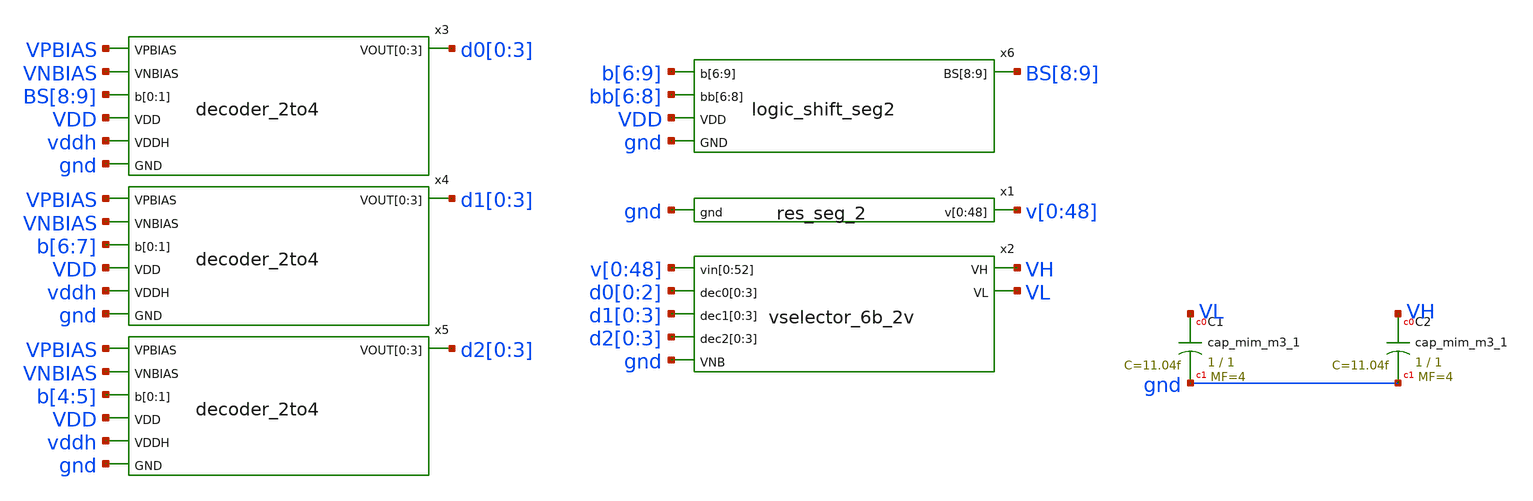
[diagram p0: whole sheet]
** sch_path: xschem/res_seg_2-tb.sch
.lib $::SKYWATER_MODELS/sky130.lib.spice tt
.include $::SKYWATER_STDCELLS/sky130_fd_sc_hd.spice

**.subckt res_seg_2-tb
x1 v[0] v[1] v[2] v[3] v[4] v[5] v[6] v[7] v[8] v[9] v[10] v[11] v[12] v[13] v[14] v[15] v[16] v[17]
+ v[18] v[19] v[20] v[21] v[22] v[23] v[24] v[25] v[26] v[27] v[28] v[29] v[30] v[31] v[32] v[33] v[34]
+ v[35] v[36] v[37] v[38] v[39] v[40] v[41] v[42] v[43] v[44] v[45] v[46] v[47] v[48] gnd res_seg_2
x2 v[0] v[1] v[2] v[3] v[4] v[5] v[6] v[7] v[8] v[9] v[10] v[11] v[12] v[13] v[14] v[15] v[16] v[17]
+ v[18] v[19] v[20] v[21] v[22] v[23] v[24] v[25] v[26] v[27] v[28] v[29] v[30] v[31] v[32] v[33] v[34]
+ v[35] v[36] v[37] v[38] v[39] v[40] v[41] v[42] v[43] v[44] v[45] v[46] v[47] v[48] v[0] v[1] v[2] v[3]
+ d0[0] d0[1] d0[2] d0[0] d1[0] d1[1] d1[2] d1[3] d2[0] d2[1] d2[2] d2[3] VH VL gnd vselector_6b_2v
XC1 VL gnd sky130_fd_pr__cap_mim_m3_1 W=1 L=1 MF=4 m=4
XC2 VH gnd sky130_fd_pr__cap_mim_m3_1 W=1 L=1 MF=4 m=4
x3 VPBIAS VNBIAS BS[8] BS[9] d0[0] d0[1] d0[2] d0[3] VDD vddh gnd decoder_2to4
x4 VPBIAS VNBIAS b[6] b[7] d1[0] d1[1] d1[2] d1[3] VDD vddh gnd decoder_2to4
x5 VPBIAS VNBIAS b[4] b[5] d2[0] d2[1] d2[2] d2[3] VDD vddh gnd decoder_2to4
x6 b[6] b[7] b[8] b[9] bb[6] bb[7] bb[8] BS[8] BS[9] VDD gnd logic_shift_seg2
**** begin user architecture code



  .option wnflag=1
  .option safecurrents
  .options reltol=1e-5
  .option klu
  ********************Static Voltage Sources***************************
  Vddh vddh gnd dc 5.5
  Vdd vdd gnd dc 1.8

  .param vpb_val = 2.98 vnb_val=1.506
  Vp vpbias gnd dc vpb_val
  Vn vnbias gnd dc vnb_val

  V52 v[48] gnd dc 4.0164
  v0 v[0] gnd dc 1.0442
  ********************Dynamic Voltage Sources***************************
  *******Calculation**********
  .param base_f=100e3 base_t={1/base_f} base_th={base_t/2} base_d={base_th}
  .param b4_th={base_th} b4_t={b4_th*2}
  .param b5_th={b4_th*2} b5_t={b5_th*2}
  .param b6_th={b5_th*2} b6_t={b6_th*2}
  .param b7_th={b6_th*2} b7_t={b7_th*2}
  .param b8_th={b7_th*2} b8_t={b8_th*2}
  .param b9_th={b8_th*2} b9_t={b9_th*2}

  .param delay_6 = {base_d+b5_t}
  .param delay_7 = {delay_6}
  .param delay_8 = {delay_7+b7_th}
  .param delay_9 = {delay_8+b8_th}
  *******Signals**********
  .param vhi=1.8
  Vb4  b[4]  gnd pulse({vhi} 0 {base_d} 1n 1n {b4_th} {b4_t})
  Vb5  b[5]  gnd pulse({vhi} 0 {base_d} 1n 1n {b5_th} {b5_t})
  Vb6  b[6]  gnd pulse({vhi} 0 {delay_6} 1n 1n {b6_th} {b6_t})
  Vb7  b[7]  gnd pulse(0 {vhi} {delay_7} 1n 1n {b7_th} {b7_t})
  Vb8  b[8]  gnd pulse(0 {vhi} {delay_8} 1n 1n {b8_th} {b8_t})
  Vb9  b[9]  gnd pulse(0 {vhi} {delay_9} 1n 1n {b9_th} {b9_t})

  Vbb4  bb[4]  gnd pulse(0 {vhi} {base_d} 1n 1n {b4_th} {b4_t})
  Vbb5  bb[5]  gnd pulse(0 {vhi} {base_d} 1n 1n {b5_th} {b5_t})
  Vbb6  bb[6]  gnd pulse(0 {vhi} {delay_6} 1n 1n {b6_th} {b6_t})
  Vbb7  bb[7]  gnd pulse({vhi} 0 {delay_7} 1n 1n {b7_th} {b7_t})
  Vbb8  bb[8]  gnd pulse({vhi} 0 {delay_8} 1n 1n {b8_th} {b8_t})
  Vbb9  bb[9]  gnd pulse({vhi} 0 {delay_9} 1n 1n {b9_th} {b9_t})
  ********************Simulation Commands*****************************
  .control
     reset
     set num_threads=50
     save all
     tran 10n 260u
     write res_seg_2-tb.raw
     set appendwrite
*    quit 0
  .endc



**** end user architecture code
**.ends

* expanding   symbol:  res_seg_2.sym # of pins=2
** sym_path: xschem/res_seg_2.sym
** sch_path: xschem/res_seg_2.sch
.subckt res_seg_2 v[0] v[1] v[2] v[3] v[4] v[5] v[6] v[7] v[8] v[9] v[10] v[11] v[12] v[13] v[14]
+ v[15] v[16] v[17] v[18] v[19] v[20] v[21] v[22] v[23] v[24] v[25] v[26] v[27] v[28] v[29] v[30] v[31]
+ v[32] v[33] v[34] v[35] v[36] v[37] v[38] v[39] v[40] v[41] v[42] v[43] v[44] v[45] v[46] v[47] v[48] gnd
*.opin
*+ v[0],v[1],v[2],v[3],v[4],v[5],v[6],v[7],v[8],v[9],v[10],v[11],v[12],v[13],v[14],v[15],v[16],v[17],v[18],v[19],v[20],v[21],v[22],v[23],v[24],v[25],v[26],v[27],v[28],v[29],v[30],v[31],v[32],v[33],v[34],v[35],v[36],v[37],v[38],v[39],v[40],v[41],v[42],v[43],v[44],v[45],v[46],v[47],v[48]
*.ipin gnd
XR1 v[1] v[0] gnd sky130_fd_pr__res_xhigh_po_0p35 L=1.9570 mult=1 m=1
XR2 v[2] v[1] gnd sky130_fd_pr__res_xhigh_po_0p35 L=1.7348 mult=1 m=1
XR3 v[3] v[2] gnd sky130_fd_pr__res_xhigh_po_0p35 L=1.5639 mult=1 m=1
XR4 v[4] v[3] gnd sky130_fd_pr__res_xhigh_po_0p35 L=1.4442 mult=1 m=1
XR5 v[5] v[4] gnd sky130_fd_pr__res_xhigh_po_0p35 L=1.3417 mult=1 m=1
XR6 v[6] v[5] gnd sky130_fd_pr__res_xhigh_po_0p35 L=1.2648 mult=1 m=1
XR7 v[7] v[6] gnd sky130_fd_pr__res_xhigh_po_0p35 L=1.1964 mult=1 m=1
XR8 v[8] v[7] gnd sky130_fd_pr__res_xhigh_po_0p35 L=1.1366 mult=1 m=1
XR9 v[9] v[8] gnd sky130_fd_pr__res_xhigh_po_0p35 L=1.0853 mult=1 m=1
XR10 v[10] v[9] gnd sky130_fd_pr__res_xhigh_po_0p35 L=1.0511 mult=1 m=1
XR11 v[11] v[10] gnd sky130_fd_pr__res_xhigh_po_0p35 L=1.0169 mult=1 m=1
XR12 v[12] v[11] gnd sky130_fd_pr__res_xhigh_po_0p35 L=0.9828 mult=1 m=1
XR13 v[13] v[12] gnd sky130_fd_pr__res_xhigh_po_0p35 L=0.9571 mult=1 m=1
XR14 v[14] v[13] gnd sky130_fd_pr__res_xhigh_po_0p35 L=0.94 mult=1 m=1
XR15 v[15] v[14] gnd sky130_fd_pr__res_xhigh_po_0p35 L=0.9144 mult=1 m=1
XR16 v[16] v[15] gnd sky130_fd_pr__res_xhigh_po_0p35 L=0.8888 mult=1 m=1
XR17 v[17] v[16] gnd sky130_fd_pr__res_xhigh_po_0p35 L=0.8802 mult=1 m=1
XR18 v[18] v[17] gnd sky130_fd_pr__res_xhigh_po_0p35 L=0.8717 mult=1 m=1
XR19 v[19] v[18] gnd sky130_fd_pr__res_xhigh_po_0p35 L=0.8546 mult=1 m=1
XR20 v[20] v[19] gnd sky130_fd_pr__res_xhigh_po_0p35 L=0.8375 mult=1 m=1
XR22 v[22] v[21] gnd sky130_fd_pr__res_xhigh_po_0p35 L=0.8289 mult=1 m=1
XR23 v[23] v[22] gnd sky130_fd_pr__res_xhigh_po_0p35 L=0.8204 mult=1 m=1
XR24 v[24] v[23] gnd sky130_fd_pr__res_xhigh_po_0p35 L=0.8118 mult=1 m=1
XR33 v[33] v[32] gnd sky130_fd_pr__res_xhigh_po_0p35 L=0.8204 mult=1 m=1
XR35 v[35] v[34] gnd sky130_fd_pr__res_xhigh_po_0p35 L=0.8289 mult=1 m=1
XR36 v[36] v[35] gnd sky130_fd_pr__res_xhigh_po_0p35 L=0.8375 mult=1 m=1
XR38 v[38] v[37] gnd sky130_fd_pr__res_xhigh_po_0p35 L=0.8631 mult=1 m=1
XR40 v[40] v[39] gnd sky130_fd_pr__res_xhigh_po_0p35 L=0.8888 mult=1 m=1
XR41 v[41] v[40] gnd sky130_fd_pr__res_xhigh_po_0p35 L=0.8973 mult=1 m=1
XR42 v[42] v[41] gnd sky130_fd_pr__res_xhigh_po_0p35 L=0.9144 mult=1 m=1
XR43 v[43] v[42] gnd sky130_fd_pr__res_xhigh_po_0p35 L=0.94 mult=1 m=1
XR44 v[44] v[43] gnd sky130_fd_pr__res_xhigh_po_0p35 L=0.9571 mult=1 m=1
XR45 v[45] v[44] gnd sky130_fd_pr__res_xhigh_po_0p35 L=0.9828 mult=1 m=1
XR46 v[46] v[45] gnd sky130_fd_pr__res_xhigh_po_0p35 L=1.0084 mult=1 m=1
XR47 v[47] v[46] gnd sky130_fd_pr__res_xhigh_po_0p35 L=1.0426 mult=1 m=1
XR48 v[48] v[47] gnd sky130_fd_pr__res_xhigh_po_0p35 L=1.0853 mult=1 m=1
XR37 v[37] v[36] gnd sky130_fd_pr__res_xhigh_po_0p35 L=0.846 mult=1 m=1
XR21 v[21] v[20] gnd sky130_fd_pr__res_xhigh_po_0p35 L=0.8375 mult=1 m=1
XR25 v[25] v[24] gnd sky130_fd_pr__res_xhigh_po_0p35 L=0.8118 mult=1 m=1
XR26 v[26] v[25] gnd sky130_fd_pr__res_xhigh_po_0p35 L=0.8118 mult=1 m=1
XR27 v[27] v[26] gnd sky130_fd_pr__res_xhigh_po_0p35 L=0.8033 mult=1 m=1
XR28 v[28] v[27] gnd sky130_fd_pr__res_xhigh_po_0p35 L=0.8118 mult=1 m=1
XR29 v[29] v[28] gnd sky130_fd_pr__res_xhigh_po_0p35 L=0.8033 mult=1 m=1
XR30 v[30] v[29] gnd sky130_fd_pr__res_xhigh_po_0p35 L=0.8033 mult=1 m=1
XR31 v[31] v[30] gnd sky130_fd_pr__res_xhigh_po_0p35 L=0.8118 mult=1 m=1
XR32 v[32] v[31] gnd sky130_fd_pr__res_xhigh_po_0p35 L=0.8118 mult=1 m=1
XR34 v[34] v[33] gnd sky130_fd_pr__res_xhigh_po_0p35 L=0.8204 mult=1 m=1
XR39 v[39] v[38] gnd sky130_fd_pr__res_xhigh_po_0p35 L=0.8631 mult=1 m=1
.ends


* expanding   symbol:  vselector_6b_2v.sym # of pins=7
** sym_path: xschem/vselector_6b_2v.sym
** sch_path: xschem/vselector_6b_2v.sch
.subckt vselector_6b_2v vin[0] vin[1] vin[2] vin[3] vin[4] vin[5] vin[6] vin[7] vin[8] vin[9]
+ vin[10] vin[11] vin[12] vin[13] vin[14] vin[15] vin[16] vin[17] vin[18] vin[19] vin[20] vin[21] vin[22]
+ vin[23] vin[24] vin[25] vin[26] vin[27] vin[28] vin[29] vin[30] vin[31] vin[32] vin[33] vin[34] vin[35]
+ vin[36] vin[37] vin[38] vin[39] vin[40] vin[41] vin[42] vin[43] vin[44] vin[45] vin[46] vin[47] vin[48]
+ vin[49] vin[50] vin[51] vin[52] dec0[0] dec0[1] dec0[2] dec0[3] dec1[0] dec1[1] dec1[2] dec1[3] dec2[0]
+ dec2[1] dec2[2] dec2[3] VH VL VNB
*.ipin
*+ vin[0],vin[1],vin[2],vin[3],vin[4],vin[5],vin[6],vin[7],vin[8],vin[9],vin[10],vin[11],vin[12],vin[13],vin[14],vin[15],vin[16],vin[17],vin[18],vin[19],vin[20],vin[21],vin[22],vin[23],vin[24],vin[25],vin[26],vin[27],vin[28],vin[29],vin[30],vin[31],vin[32],vin[33],vin[34],vin[35],vin[36],vin[37],vin[38],vin[39],vin[40],vin[41],vin[42],vin[43],vin[44],vin[45],vin[46],vin[47],vin[48],vin[49],vin[50],vin[51],vin[52]
*.opin VH
*.ipin VNB
*.ipin dec0[0],dec0[1],dec0[2],dec0[3]
*.opin VL
*.ipin dec1[0],dec1[1],dec1[2],dec1[3]
*.ipin dec2[0],dec2[1],dec2[2],dec2[3]
x1 vin[0] vin[1] vin[2] vin[3] vin[4] vin[5] vin[6] vin[7] vin[8] vin[9] vin[10] vin[11] vin[12]
+ vin[13] vin[14] vin[15] vin[16] vin[17] vin[18] vin[19] vin[20] vin[21] vin[22] vin[23] vin[24] vin[25]
+ vin[26] vin[27] vin[28] vin[29] vin[30] vin[31] vin[32] vin[33] vin[34] vin[35] vin[36] vin[37] vin[38]
+ vin[39] vin[40] vin[41] vin[42] vin[43] vin[44] vin[45] vin[46] vin[47] vin[48] vin[49] vin[50] vin[51]
+ vin[52] dec0[0] dec0[1] dec0[2] dec0[3] dec0[0] vout1[0] vout1[1] vout1[2] vout1[3] vout1[4] vout1[5]
+ vout1[6] vout1[7] vout1[8] vout1[9] vout1[10] vout1[11] vout1[12] vout1[13] vout1[14] vout1[15] vout1[16]
+ VNB vselector_6b_2v_stage_1
x2 vout1[0] vout1[1] vout1[2] vout1[3] vout1[4] vout1[5] vout1[6] vout1[7] vout1[8] vout1[9]
+ vout1[10] vout1[11] vout1[12] vout1[13] vout1[14] vout1[15] vout1[16] dec1[0] dec1[1] dec1[2] dec1[3]
+ vout2[0] vout2[1] vout2[2] vout2[3] vout2[4] VNB vselector_6b_2v_stage_2
x3 vout2[0] vout2[1] vout2[2] vout2[3] vout2[4] dec2[0] dec2[1] dec2[2] dec2[3] VH VL VNB
+ vselector_6b_2v_stage_3
XC1 VL VNB sky130_fd_pr__cap_mim_m3_1 W=1 L=1 MF=8 m=8
XC2 VH VNB sky130_fd_pr__cap_mim_m3_1 W=1 L=1 MF=8 m=8
.ends


* expanding   symbol:  decoder_2to4.sym # of pins=7
** sym_path: xschem/decoder_2to4.sym
** sch_path: xschem/decoder_2to4.sch
.subckt decoder_2to4 VPBIAS VNBIAS b[0] b[1] VOUT[0] VOUT[1] VOUT[2] VOUT[3] VDD VDDH GND
*.ipin VPBIAS
*.ipin VNBIAS
*.ipin b[0],b[1]
*.opin VOUT[0],VOUT[1],VOUT[2],VOUT[3]
*.ipin VDDH
*.ipin GND
*.ipin VDD
x1 VPBIAS VNBIAS DIN[0] VOUT[1] VOUT[2] VOUT[3] VOUT[0] VDDH GND VDDH GND pull_up_down_network
x2 VPBIAS VNBIAS DIN[1] VOUT[0] VOUT[2] VOUT[3] VOUT[1] VDDH GND VDDH GND pull_up_down_network
x3 VPBIAS VNBIAS DIN[2] VOUT[0] VOUT[1] VOUT[3] VOUT[2] VDDH GND VDDH GND pull_up_down_network
x4 VPBIAS VNBIAS DIN[3] VOUT[0] VOUT[1] VOUT[2] VOUT[3] VDDH GND VDDH GND pull_up_down_network
x6 bb[0] bb[1] DIN[0] VDD GND nand
x7 b[0] bb[1] DIN[1] VDD GND nand
x8 bb[0] b[1] DIN[2] VDD GND nand
x9 b[0] b[1] DIN[3] VDD GND nand
x5 b[0] bb[0] VDD GND inv
x10 b[1] bb[1] VDD GND inv
.ends


* expanding   symbol:  logic_shift_seg2.sym # of pins=5
** sym_path: xschem/logic_shift_seg2.sym
** sch_path: xschem/logic_shift_seg2.sch
.subckt logic_shift_seg2 b[6] b[7] b[8] b[9] bb[6] bb[7] bb[8] BS[8] BS[9] VDD GND
*.ipin b[6],b[7],b[8],b[9]
*.opin BS[8],BS[9]
*.ipin GND
*.ipin VDD
*.ipin bb[6],bb[7],bb[8]
x1 b[9] b[8] GND GND VDD VDD n1 sky130_fd_sc_hd__nand2_1
x2 b[9] b[7] GND GND VDD VDD n2 sky130_fd_sc_hd__nand2_1
x3 b[9] b[6] GND GND VDD VDD n3 sky130_fd_sc_hd__nand2_1
x5 bb[8] bb[7] bb[6] GND GND VDD VDD n6 sky130_fd_sc_hd__nand3_1
x4 n3 n2 n1 GND GND VDD VDD BS[9] sky130_fd_sc_hd__nand3_1
x6 b[6] b[8] GND GND VDD VDD n4 sky130_fd_sc_hd__nand2_1
x7 b[7] b[8] GND GND VDD VDD n5 sky130_fd_sc_hd__nand2_1
x8 n6 n5 n4 GND GND VDD VDD BS[8] sky130_fd_sc_hd__nand3_1
.ends


* expanding   symbol:  vselector_6b_2v_stage_1.sym # of pins=4
** sym_path: xschem/vselector_6b_2v_stage_1.sym
** sch_path: xschem/vselector_6b_2v_stage_1.sch
.subckt vselector_6b_2v_stage_1 vin[0] vin[1] vin[2] vin[3] vin[4] vin[5] vin[6] vin[7] vin[8]
+ vin[9] vin[10] vin[11] vin[12] vin[13] vin[14] vin[15] vin[16] vin[17] vin[18] vin[19] vin[20] vin[21]
+ vin[22] vin[23] vin[24] vin[25] vin[26] vin[27] vin[28] vin[29] vin[30] vin[31] vin[32] vin[33] vin[34]
+ vin[35] vin[36] vin[37] vin[38] vin[39] vin[40] vin[41] vin[42] vin[43] vin[44] vin[45] vin[46] vin[47]
+ vin[48] vin[49] vin[50] vin[51] vin[52] dec[0] dec[1] dec[2] dec[3] dec[4] vout[0] vout[1] vout[2] vout[3]
+ vout[4] vout[5] vout[6] vout[7] vout[8] vout[9] vout[10] vout[11] vout[12] vout[13] vout[14] vout[15]
+ vout[16] VNB
*.ipin
*+ vin[0],vin[1],vin[2],vin[3],vin[4],vin[5],vin[6],vin[7],vin[8],vin[9],vin[10],vin[11],vin[12],vin[13],vin[14],vin[15],vin[16],vin[17],vin[18],vin[19],vin[20],vin[21],vin[22],vin[23],vin[24],vin[25],vin[26],vin[27],vin[28],vin[29],vin[30],vin[31],vin[32],vin[33],vin[34],vin[35],vin[36],vin[37],vin[38],vin[39],vin[40],vin[41],vin[42],vin[43],vin[44],vin[45],vin[46],vin[47],vin[48],vin[49],vin[50],vin[51],vin[52]
*.opin
*+ vout[0],vout[1],vout[2],vout[3],vout[4],vout[5],vout[6],vout[7],vout[8],vout[9],vout[10],vout[11],vout[12],vout[13],vout[14],vout[15],vout[16]
*.ipin VNB
*.ipin dec[0],dec[1],dec[2],dec[3],dec[4]
x1 vin[0] vin[1] vin[2] vin[3] vin[4] vin[5] vin[6] vin[7] vin[8] vin[9] vin[10] vin[11] vin[12]
+ vin[13] vin[14] vin[15] vin[16] dec[0] vout[0] vout[1] vout[2] vout[3] vout[4] vout[5] vout[6] vout[7]
+ vout[8] vout[9] vout[10] vout[11] vout[12] vout[13] vout[14] vout[15] vout[16] VNB vselector_16b
x2 vin[16] vin[17] vin[18] vin[19] vin[20] vin[21] vin[22] vin[23] vin[24] vin[25] vin[26] vin[27]
+ vin[28] vin[29] vin[30] vin[31] vin[32] dec[1] vout[0] vout[1] vout[2] vout[3] vout[4] vout[5] vout[6]
+ vout[7] vout[8] vout[9] vout[10] vout[11] vout[12] vout[13] vout[14] vout[15] vout[16] VNB vselector_16b
x3 vin[32] vin[33] vin[34] vin[35] vin[36] vin[37] vin[38] vin[39] vin[40] vin[41] vin[42] vin[43]
+ vin[44] vin[45] vin[46] vin[47] vin[48] dec[2] vout[0] vout[1] vout[2] vout[3] vout[4] vout[5] vout[6]
+ vout[7] vout[8] vout[9] vout[10] vout[11] vout[12] vout[13] vout[14] vout[15] vout[16] VNB vselector_16b
x4 vin[48] vin[49] vin[50] vin[51] vin[52] dec[3] vout[0] vout[1] vout[2] vout[3] vout[4] VNB
+ vselector_4b
.ends


* expanding   symbol:  vselector_6b_2v_stage_2.sym # of pins=4
** sym_path: xschem/vselector_6b_2v_stage_2.sym
** sch_path: xschem/vselector_6b_2v_stage_2.sch
.subckt vselector_6b_2v_stage_2 vin[0] vin[1] vin[2] vin[3] vin[4] vin[5] vin[6] vin[7] vin[8]
+ vin[9] vin[10] vin[11] vin[12] vin[13] vin[14] vin[15] vin[16] dec[0] dec[1] dec[2] dec[3] vout[0] vout[1]
+ vout[2] vout[3] vout[4] VNB
*.ipin
*+ vin[0],vin[1],vin[2],vin[3],vin[4],vin[5],vin[6],vin[7],vin[8],vin[9],vin[10],vin[11],vin[12],vin[13],vin[14],vin[15],vin[16]
*.opin vout[0],vout[1],vout[2],vout[3],vout[4]
*.ipin VNB
*.ipin dec[0],dec[1],dec[2],dec[3]
x1 vin[0] vin[1] vin[2] vin[3] vin[4] dec[0] vout[0] vout[1] vout[2] vout[3] vout[4] VNB
+ vselector_4b
x2 vin[4] vin[5] vin[6] vin[7] vin[8] dec[1] vout[0] vout[1] vout[2] vout[3] vout[4] VNB
+ vselector_4b
x3 vin[8] vin[9] vin[10] vin[11] vin[12] dec[2] vout[0] vout[1] vout[2] vout[3] vout[4] VNB
+ vselector_4b
x4 vin[12] vin[13] vin[14] vin[15] vin[16] dec[3] vout[0] vout[1] vout[2] vout[3] vout[4] VNB
+ vselector_4b
.ends


* expanding   symbol:  vselector_6b_2v_stage_3.sym # of pins=5
** sym_path: xschem/vselector_6b_2v_stage_3.sym
** sch_path: xschem/vselector_6b_2v_stage_3.sch
.subckt vselector_6b_2v_stage_3 vin[0] vin[1] vin[2] vin[3] vin[4] dec[0] dec[1] dec[2] dec[3] VH VL
+ VNB
*.ipin vin[0],vin[1],vin[2],vin[3],vin[4]
*.opin VH
*.ipin VNB
*.ipin dec[0],dec[1],dec[2],dec[3]
*.opin VL
x1 vin[0] vin[1] dec[0] VH VL VNB vselector_1b
x2 vin[1] vin[2] dec[1] VH VL VNB vselector_1b
x3 vin[2] vin[3] dec[2] VH VL VNB vselector_1b
x4 vin[3] vin[4] dec[3] VH VL VNB vselector_1b
.ends


* expanding   symbol:  pull_up_down_network.sym # of pins=9
** sym_path: xschem/pull_up_down_network.sym
** sch_path: xschem/pull_up_down_network.sch
.subckt pull_up_down_network VPBIAS VNBIAS DIN V[0] V[1] V[2] VOUT VDDH GND VPB VNB
*.ipin VPBIAS
*.ipin VNBIAS
*.ipin DIN
*.ipin V[0],V[1],V[2]
*.opin VOUT
*.ipin VDDH
*.ipin GND
*.ipin VPB
*.ipin VNB
XM1 net2 VPBIAS VDDH VPB sky130_fd_pr__pfet_g5v0d10v5 L=l W=wp nf=1 ad='int((nf+1)/2) * W/nf * 0.29'
+ as='int((nf+2)/2) * W/nf * 0.29' pd='2*int((nf+1)/2) * (W/nf + 0.29)' ps='2*int((nf+2)/2) * (W/nf + 0.29)'
+ nrd='0.29 / W' nrs='0.29 / W' sa=0 sb=0 sd=0 mult=1 m=1
.param wp=0.84 wn=1 l=1

XM2 net3 V[0] net2 VPB sky130_fd_pr__pfet_g5v0d10v5 L=l W=wp nf=1 ad='int((nf+1)/2) * W/nf * 0.29' as='int((nf+2)/2) * W/nf * 0.29'
+ pd='2*int((nf+1)/2) * (W/nf + 0.29)' ps='2*int((nf+2)/2) * (W/nf + 0.29)' nrd='0.29 / W' nrs='0.29 / W'
+ sa=0 sb=0 sd=0 mult=1 m=1
XM3 net4 V[1] net3 VPB sky130_fd_pr__pfet_g5v0d10v5 L=l W=wp nf=1 ad='int((nf+1)/2) * W/nf * 0.29' as='int((nf+2)/2) * W/nf * 0.29'
+ pd='2*int((nf+1)/2) * (W/nf + 0.29)' ps='2*int((nf+2)/2) * (W/nf + 0.29)' nrd='0.29 / W' nrs='0.29 / W'
+ sa=0 sb=0 sd=0 mult=1 m=1
XM4 VOUT V[2] net4 VPB sky130_fd_pr__pfet_g5v0d10v5 L=l W=wp nf=1 ad='int((nf+1)/2) * W/nf * 0.29' as='int((nf+2)/2) * W/nf * 0.29'
+ pd='2*int((nf+1)/2) * (W/nf + 0.29)' ps='2*int((nf+2)/2) * (W/nf + 0.29)' nrd='0.29 / W' nrs='0.29 / W'
+ sa=0 sb=0 sd=0 mult=1 m=1
XM5 VOUT VNBIAS net1 VNB sky130_fd_pr__nfet_g5v0d10v5 L=l W=wn nf=1 ad='int((nf+1)/2) * W/nf * 0.29'
+ as='int((nf+2)/2) * W/nf * 0.29' pd='2*int((nf+1)/2) * (W/nf + 0.29)' ps='2*int((nf+2)/2) * (W/nf + 0.29)'
+ nrd='0.29 / W' nrs='0.29 / W' sa=0 sb=0 sd=0 mult=1 m=1
XM6 net1 DIN GND VNB sky130_fd_pr__nfet_01v8 L=0.15 W=2 nf=1 ad='int((nf+1)/2) * W/nf * 0.29' as='int((nf+2)/2) * W/nf * 0.29'
+ pd='2*int((nf+1)/2) * (W/nf + 0.29)' ps='2*int((nf+2)/2) * (W/nf + 0.29)' nrd='0.29 / W' nrs='0.29 / W'
+ sa=0 sb=0 sd=0 mult=1 m=1
.ends


* expanding   symbol:  nand.sym # of pins=5
** sym_path: xschem/nand.sym
** sch_path: xschem/nand.sch
.subckt nand in1 in2 out VDD GND
*.ipin in2
*.opin out
*.ipin VDD
*.ipin GND
*.ipin in1
.param wp=0.63 wn=0.42 l=0.15
XM1 out in1 VDD VDD sky130_fd_pr__pfet_01v8 L=l W=wp nf=1 ad='int((nf+1)/2) * W/nf * 0.29' as='int((nf+2)/2) * W/nf * 0.29'
+ pd='2*int((nf+1)/2) * (W/nf + 0.29)' ps='2*int((nf+2)/2) * (W/nf + 0.29)' nrd='0.29 / W' nrs='0.29 / W'
+ sa=0 sb=0 sd=0 mult=1 m=1
XM2 out in2 VDD VDD sky130_fd_pr__pfet_01v8 L=l W=wp nf=1 ad='int((nf+1)/2) * W/nf * 0.29' as='int((nf+2)/2) * W/nf * 0.29'
+ pd='2*int((nf+1)/2) * (W/nf + 0.29)' ps='2*int((nf+2)/2) * (W/nf + 0.29)' nrd='0.29 / W' nrs='0.29 / W'
+ sa=0 sb=0 sd=0 mult=1 m=1
XM3 out in2 net1 GND sky130_fd_pr__nfet_01v8 L=l W=wn nf=1 ad='int((nf+1)/2) * W/nf * 0.29' as='int((nf+2)/2) * W/nf * 0.29'
+ pd='2*int((nf+1)/2) * (W/nf + 0.29)' ps='2*int((nf+2)/2) * (W/nf + 0.29)' nrd='0.29 / W' nrs='0.29 / W'
+ sa=0 sb=0 sd=0 mult=1 m=1
XM4 net1 in1 GND GND sky130_fd_pr__nfet_01v8 L=l W=wn nf=1 ad='int((nf+1)/2) * W/nf * 0.29' as='int((nf+2)/2) * W/nf * 0.29'
+ pd='2*int((nf+1)/2) * (W/nf + 0.29)' ps='2*int((nf+2)/2) * (W/nf + 0.29)' nrd='0.29 / W' nrs='0.29 / W'
+ sa=0 sb=0 sd=0 mult=1 m=1
.ends


* expanding   symbol:  inv.sym # of pins=4
** sym_path: xschem/inv.sym
** sch_path: xschem/inv.sch
.subckt inv in out vdd gnd
*.ipin in
*.opin out
*.ipin vdd
*.ipin gnd
XM1 out in gnd gnd sky130_fd_pr__nfet_01v8 L=0.15 W=0.42 nf=1 ad='int((nf+1)/2) * W/nf * 0.29' as='int((nf+2)/2) * W/nf * 0.29'
+ pd='2*int((nf+1)/2) * (W/nf + 0.29)' ps='2*int((nf+2)/2) * (W/nf + 0.29)' nrd='0.29 / W' nrs='0.29 / W'
+ sa=0 sb=0 sd=0 mult=1 m=1
XM2 out in vdd vdd sky130_fd_pr__pfet_01v8 L=0.15 W=1.26 nf=1 ad='int((nf+1)/2) * W/nf * 0.29' as='int((nf+2)/2) * W/nf * 0.29'
+ pd='2*int((nf+1)/2) * (W/nf + 0.29)' ps='2*int((nf+2)/2) * (W/nf + 0.29)' nrd='0.29 / W' nrs='0.29 / W'
+ sa=0 sb=0 sd=0 mult=1 m=1
.ends


* expanding   symbol:  vselector_16b.sym # of pins=4
** sym_path: xschem/vselector_16b.sym
** sch_path: xschem/vselector_16b.sch
.subckt vselector_16b vin[0] vin[1] vin[2] vin[3] vin[4] vin[5] vin[6] vin[7] vin[8] vin[9] vin[10]
+ vin[11] vin[12] vin[13] vin[14] vin[15] vin[16] DIN vout[0] vout[1] vout[2] vout[3] vout[4] vout[5] vout[6]
+ vout[7] vout[8] vout[9] vout[10] vout[11] vout[12] vout[13] vout[14] vout[15] vout[16] VNB
*.ipin
*+ vin[0],vin[1],vin[2],vin[3],vin[4],vin[5],vin[6],vin[7],vin[8],vin[9],vin[10],vin[11],vin[12],vin[13],vin[14],vin[15],vin[16]
*.opin
*+ vout[0],vout[1],vout[2],vout[3],vout[4],vout[5],vout[6],vout[7],vout[8],vout[9],vout[10],vout[11],vout[12],vout[13],vout[14],vout[15],vout[16]
*.ipin VNB
*.ipin DIN
XM1 vout[0] DIN vin[0] VNB sky130_fd_pr__nfet_g5v0d10v5 L=l W=wn nf=1 ad='int((nf+1)/2) * W/nf * 0.29'
+ as='int((nf+2)/2) * W/nf * 0.29' pd='2*int((nf+1)/2) * (W/nf + 0.29)' ps='2*int((nf+2)/2) * (W/nf + 0.29)'
+ nrd='0.29 / W' nrs='0.29 / W' sa=0 sb=0 sd=0 mult=1 m=1
XM2 vout[1] DIN vin[1] VNB sky130_fd_pr__nfet_g5v0d10v5 L=l W=wn nf=1 ad='int((nf+1)/2) * W/nf * 0.29'
+ as='int((nf+2)/2) * W/nf * 0.29' pd='2*int((nf+1)/2) * (W/nf + 0.29)' ps='2*int((nf+2)/2) * (W/nf + 0.29)'
+ nrd='0.29 / W' nrs='0.29 / W' sa=0 sb=0 sd=0 mult=1 m=1
XM3 vout[2] DIN vin[2] VNB sky130_fd_pr__nfet_g5v0d10v5 L=l W=wn nf=1 ad='int((nf+1)/2) * W/nf * 0.29'
+ as='int((nf+2)/2) * W/nf * 0.29' pd='2*int((nf+1)/2) * (W/nf + 0.29)' ps='2*int((nf+2)/2) * (W/nf + 0.29)'
+ nrd='0.29 / W' nrs='0.29 / W' sa=0 sb=0 sd=0 mult=1 m=1
XM4 vout[3] DIN vin[3] VNB sky130_fd_pr__nfet_g5v0d10v5 L=l W=wn nf=1 ad='int((nf+1)/2) * W/nf * 0.29'
+ as='int((nf+2)/2) * W/nf * 0.29' pd='2*int((nf+1)/2) * (W/nf + 0.29)' ps='2*int((nf+2)/2) * (W/nf + 0.29)'
+ nrd='0.29 / W' nrs='0.29 / W' sa=0 sb=0 sd=0 mult=1 m=1
XM5 vout[4] DIN vin[4] VNB sky130_fd_pr__nfet_g5v0d10v5 L=l W=wn nf=1 ad='int((nf+1)/2) * W/nf * 0.29'
+ as='int((nf+2)/2) * W/nf * 0.29' pd='2*int((nf+1)/2) * (W/nf + 0.29)' ps='2*int((nf+2)/2) * (W/nf + 0.29)'
+ nrd='0.29 / W' nrs='0.29 / W' sa=0 sb=0 sd=0 mult=1 m=1
XM6 vout[5] DIN vin[5] VNB sky130_fd_pr__nfet_g5v0d10v5 L=l W=wn nf=1 ad='int((nf+1)/2) * W/nf * 0.29'
+ as='int((nf+2)/2) * W/nf * 0.29' pd='2*int((nf+1)/2) * (W/nf + 0.29)' ps='2*int((nf+2)/2) * (W/nf + 0.29)'
+ nrd='0.29 / W' nrs='0.29 / W' sa=0 sb=0 sd=0 mult=1 m=1
XM7 vout[6] DIN vin[6] VNB sky130_fd_pr__nfet_g5v0d10v5 L=l W=wn nf=1 ad='int((nf+1)/2) * W/nf * 0.29'
+ as='int((nf+2)/2) * W/nf * 0.29' pd='2*int((nf+1)/2) * (W/nf + 0.29)' ps='2*int((nf+2)/2) * (W/nf + 0.29)'
+ nrd='0.29 / W' nrs='0.29 / W' sa=0 sb=0 sd=0 mult=1 m=1
XM8 vout[7] DIN vin[7] VNB sky130_fd_pr__nfet_g5v0d10v5 L=l W=wn nf=1 ad='int((nf+1)/2) * W/nf * 0.29'
+ as='int((nf+2)/2) * W/nf * 0.29' pd='2*int((nf+1)/2) * (W/nf + 0.29)' ps='2*int((nf+2)/2) * (W/nf + 0.29)'
+ nrd='0.29 / W' nrs='0.29 / W' sa=0 sb=0 sd=0 mult=1 m=1
XM9 vout[8] DIN vin[8] VNB sky130_fd_pr__nfet_g5v0d10v5 L=l W=wn nf=1 ad='int((nf+1)/2) * W/nf * 0.29'
+ as='int((nf+2)/2) * W/nf * 0.29' pd='2*int((nf+1)/2) * (W/nf + 0.29)' ps='2*int((nf+2)/2) * (W/nf + 0.29)'
+ nrd='0.29 / W' nrs='0.29 / W' sa=0 sb=0 sd=0 mult=1 m=1
XM10 vout[9] DIN vin[9] VNB sky130_fd_pr__nfet_g5v0d10v5 L=l W=wn nf=1 ad='int((nf+1)/2) * W/nf * 0.29'
+ as='int((nf+2)/2) * W/nf * 0.29' pd='2*int((nf+1)/2) * (W/nf + 0.29)' ps='2*int((nf+2)/2) * (W/nf + 0.29)'
+ nrd='0.29 / W' nrs='0.29 / W' sa=0 sb=0 sd=0 mult=1 m=1
XM11 vout[10] DIN vin[10] VNB sky130_fd_pr__nfet_g5v0d10v5 L=l W=wn nf=1 ad='int((nf+1)/2) * W/nf * 0.29'
+ as='int((nf+2)/2) * W/nf * 0.29' pd='2*int((nf+1)/2) * (W/nf + 0.29)' ps='2*int((nf+2)/2) * (W/nf + 0.29)'
+ nrd='0.29 / W' nrs='0.29 / W' sa=0 sb=0 sd=0 mult=1 m=1
XM12 vout[11] DIN vin[11] VNB sky130_fd_pr__nfet_g5v0d10v5 L=l W=wn nf=1 ad='int((nf+1)/2) * W/nf * 0.29'
+ as='int((nf+2)/2) * W/nf * 0.29' pd='2*int((nf+1)/2) * (W/nf + 0.29)' ps='2*int((nf+2)/2) * (W/nf + 0.29)'
+ nrd='0.29 / W' nrs='0.29 / W' sa=0 sb=0 sd=0 mult=1 m=1
XM13 vout[12] DIN vin[12] VNB sky130_fd_pr__nfet_g5v0d10v5 L=l W=wn nf=1 ad='int((nf+1)/2) * W/nf * 0.29'
+ as='int((nf+2)/2) * W/nf * 0.29' pd='2*int((nf+1)/2) * (W/nf + 0.29)' ps='2*int((nf+2)/2) * (W/nf + 0.29)'
+ nrd='0.29 / W' nrs='0.29 / W' sa=0 sb=0 sd=0 mult=1 m=1
XM14 vout[13] DIN vin[13] VNB sky130_fd_pr__nfet_g5v0d10v5 L=l W=wn nf=1 ad='int((nf+1)/2) * W/nf * 0.29'
+ as='int((nf+2)/2) * W/nf * 0.29' pd='2*int((nf+1)/2) * (W/nf + 0.29)' ps='2*int((nf+2)/2) * (W/nf + 0.29)'
+ nrd='0.29 / W' nrs='0.29 / W' sa=0 sb=0 sd=0 mult=1 m=1
XM15 vout[14] DIN vin[14] VNB sky130_fd_pr__nfet_g5v0d10v5 L=l W=wn nf=1 ad='int((nf+1)/2) * W/nf * 0.29'
+ as='int((nf+2)/2) * W/nf * 0.29' pd='2*int((nf+1)/2) * (W/nf + 0.29)' ps='2*int((nf+2)/2) * (W/nf + 0.29)'
+ nrd='0.29 / W' nrs='0.29 / W' sa=0 sb=0 sd=0 mult=1 m=1
XM16 vout[15] DIN vin[15] VNB sky130_fd_pr__nfet_g5v0d10v5 L=l W=wn nf=1 ad='int((nf+1)/2) * W/nf * 0.29'
+ as='int((nf+2)/2) * W/nf * 0.29' pd='2*int((nf+1)/2) * (W/nf + 0.29)' ps='2*int((nf+2)/2) * (W/nf + 0.29)'
+ nrd='0.29 / W' nrs='0.29 / W' sa=0 sb=0 sd=0 mult=1 m=1
XM17 vout[16] DIN vin[16] VNB sky130_fd_pr__nfet_g5v0d10v5 L=l W=wn nf=1 ad='int((nf+1)/2) * W/nf * 0.29'
+ as='int((nf+2)/2) * W/nf * 0.29' pd='2*int((nf+1)/2) * (W/nf + 0.29)' ps='2*int((nf+2)/2) * (W/nf + 0.29)'
+ nrd='0.29 / W' nrs='0.29 / W' sa=0 sb=0 sd=0 mult=1 m=1
.ends


* expanding   symbol:  vselector_4b.sym # of pins=4
** sym_path: xschem/vselector_4b.sym
** sch_path: xschem/vselector_4b.sch
.subckt vselector_4b vin[0] vin[1] vin[2] vin[3] vin[4] DIN vout[0] vout[1] vout[2] vout[3] vout[4]
+ VNB
*.ipin vin[0],vin[1],vin[2],vin[3],vin[4]
*.opin vout[0],vout[1],vout[2],vout[3],vout[4]
*.ipin VNB
*.ipin DIN
XM1 vout[0] DIN vin[0] VNB sky130_fd_pr__nfet_g5v0d10v5 L=l W=wn nf=1 ad='int((nf+1)/2) * W/nf * 0.29'
+ as='int((nf+2)/2) * W/nf * 0.29' pd='2*int((nf+1)/2) * (W/nf + 0.29)' ps='2*int((nf+2)/2) * (W/nf + 0.29)'
+ nrd='0.29 / W' nrs='0.29 / W' sa=0 sb=0 sd=0 mult=1 m=1
XM2 vout[1] DIN vin[1] VNB sky130_fd_pr__nfet_g5v0d10v5 L=l W=wn nf=1 ad='int((nf+1)/2) * W/nf * 0.29'
+ as='int((nf+2)/2) * W/nf * 0.29' pd='2*int((nf+1)/2) * (W/nf + 0.29)' ps='2*int((nf+2)/2) * (W/nf + 0.29)'
+ nrd='0.29 / W' nrs='0.29 / W' sa=0 sb=0 sd=0 mult=1 m=1
XM3 vout[2] DIN vin[2] VNB sky130_fd_pr__nfet_g5v0d10v5 L=l W=wn nf=1 ad='int((nf+1)/2) * W/nf * 0.29'
+ as='int((nf+2)/2) * W/nf * 0.29' pd='2*int((nf+1)/2) * (W/nf + 0.29)' ps='2*int((nf+2)/2) * (W/nf + 0.29)'
+ nrd='0.29 / W' nrs='0.29 / W' sa=0 sb=0 sd=0 mult=1 m=1
XM4 vout[3] DIN vin[3] VNB sky130_fd_pr__nfet_g5v0d10v5 L=l W=wn nf=1 ad='int((nf+1)/2) * W/nf * 0.29'
+ as='int((nf+2)/2) * W/nf * 0.29' pd='2*int((nf+1)/2) * (W/nf + 0.29)' ps='2*int((nf+2)/2) * (W/nf + 0.29)'
+ nrd='0.29 / W' nrs='0.29 / W' sa=0 sb=0 sd=0 mult=1 m=1
XM5 vout[4] DIN vin[4] VNB sky130_fd_pr__nfet_g5v0d10v5 L=l W=wn nf=1 ad='int((nf+1)/2) * W/nf * 0.29'
+ as='int((nf+2)/2) * W/nf * 0.29' pd='2*int((nf+1)/2) * (W/nf + 0.29)' ps='2*int((nf+2)/2) * (W/nf + 0.29)'
+ nrd='0.29 / W' nrs='0.29 / W' sa=0 sb=0 sd=0 mult=1 m=1
.ends


* expanding   symbol:  vselector_1b.sym # of pins=5
** sym_path: xschem/vselector_1b.sym
** sch_path: xschem/vselector_1b.sch
.subckt vselector_1b vin[0] vin[1] DIN VH VL VNB
*.ipin vin[0],vin[1]
*.opin VL
*.ipin VNB
*.ipin DIN
*.opin VH
.param wp=0.42 wn=0.42 l=0.5

XM1 VL DIN vin[0] VNB sky130_fd_pr__nfet_g5v0d10v5 L=l W=wn nf=1 ad='int((nf+1)/2) * W/nf * 0.29' as='int((nf+2)/2) * W/nf * 0.29'
+ pd='2*int((nf+1)/2) * (W/nf + 0.29)' ps='2*int((nf+2)/2) * (W/nf + 0.29)' nrd='0.29 / W' nrs='0.29 / W'
+ sa=0 sb=0 sd=0 mult=1 m=1
XM2 VH DIN vin[1] VNB sky130_fd_pr__nfet_g5v0d10v5 L=l W=wn nf=1 ad='int((nf+1)/2) * W/nf * 0.29' as='int((nf+2)/2) * W/nf * 0.29'
+ pd='2*int((nf+1)/2) * (W/nf + 0.29)' ps='2*int((nf+2)/2) * (W/nf + 0.29)' nrd='0.29 / W' nrs='0.29 / W'
+ sa=0 sb=0 sd=0 mult=1 m=1
.ends

.end
